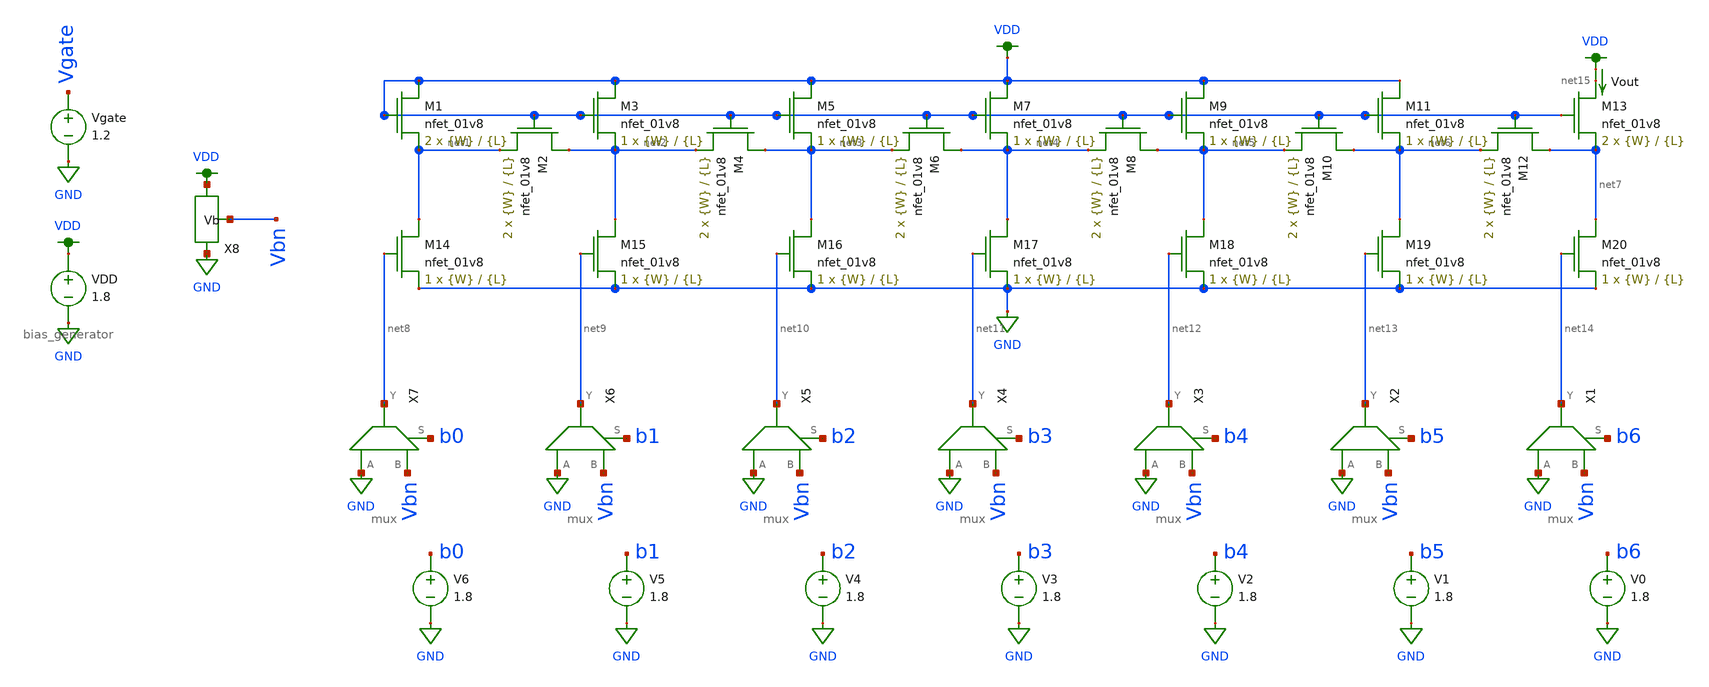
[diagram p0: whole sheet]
** sch_path: dac/schematics/misc/dac_dnl_inl.sch
**.subckt dac_dnl_inl
XM1 VDD VDD net1 GND sky130_fd_pr__nfet_01v8 L={L} W={W} nf=1 ad='int((nf+1)/2) * W/nf * 0.29' as='int((nf+2)/2) * W/nf * 0.29'
+ pd='2*int((nf+1)/2) * (W/nf + 0.29)' ps='2*int((nf+2)/2) * (W/nf + 0.29)' nrd='0.29 / W' nrs='0.29 / W'
+ sa=0 sb=0 sd=0 mult=2 m=2
XM2 net2 VDD net1 GND sky130_fd_pr__nfet_01v8 L={L} W={W} nf=1 ad='int((nf+1)/2) * W/nf * 0.29' as='int((nf+2)/2) * W/nf * 0.29'
+ pd='2*int((nf+1)/2) * (W/nf + 0.29)' ps='2*int((nf+2)/2) * (W/nf + 0.29)' nrd='0.29 / W' nrs='0.29 / W'
+ sa=0 sb=0 sd=0 mult=2 m=2
XM3 VDD VDD net2 GND sky130_fd_pr__nfet_01v8 L={L} W={W} nf=1 ad='int((nf+1)/2) * W/nf * 0.29' as='int((nf+2)/2) * W/nf * 0.29'
+ pd='2*int((nf+1)/2) * (W/nf + 0.29)' ps='2*int((nf+2)/2) * (W/nf + 0.29)' nrd='0.29 / W' nrs='0.29 / W'
+ sa=0 sb=0 sd=0 mult=1 m=1
XM4 net3 VDD net2 GND sky130_fd_pr__nfet_01v8 L={L} W={W} nf=1 ad='int((nf+1)/2) * W/nf * 0.29' as='int((nf+2)/2) * W/nf * 0.29'
+ pd='2*int((nf+1)/2) * (W/nf + 0.29)' ps='2*int((nf+2)/2) * (W/nf + 0.29)' nrd='0.29 / W' nrs='0.29 / W'
+ sa=0 sb=0 sd=0 mult=2 m=2
XM5 VDD VDD net3 GND sky130_fd_pr__nfet_01v8 L={L} W={W} nf=1 ad='int((nf+1)/2) * W/nf * 0.29' as='int((nf+2)/2) * W/nf * 0.29'
+ pd='2*int((nf+1)/2) * (W/nf + 0.29)' ps='2*int((nf+2)/2) * (W/nf + 0.29)' nrd='0.29 / W' nrs='0.29 / W'
+ sa=0 sb=0 sd=0 mult=1 m=1
XM6 net4 VDD net3 GND sky130_fd_pr__nfet_01v8 L={L} W={W} nf=1 ad='int((nf+1)/2) * W/nf * 0.29' as='int((nf+2)/2) * W/nf * 0.29'
+ pd='2*int((nf+1)/2) * (W/nf + 0.29)' ps='2*int((nf+2)/2) * (W/nf + 0.29)' nrd='0.29 / W' nrs='0.29 / W'
+ sa=0 sb=0 sd=0 mult=2 m=2
XM7 VDD VDD net4 GND sky130_fd_pr__nfet_01v8 L={L} W={W} nf=1 ad='int((nf+1)/2) * W/nf * 0.29' as='int((nf+2)/2) * W/nf * 0.29'
+ pd='2*int((nf+1)/2) * (W/nf + 0.29)' ps='2*int((nf+2)/2) * (W/nf + 0.29)' nrd='0.29 / W' nrs='0.29 / W'
+ sa=0 sb=0 sd=0 mult=1 m=1
XM8 net5 VDD net4 GND sky130_fd_pr__nfet_01v8 L={L} W={W} nf=1 ad='int((nf+1)/2) * W/nf * 0.29' as='int((nf+2)/2) * W/nf * 0.29'
+ pd='2*int((nf+1)/2) * (W/nf + 0.29)' ps='2*int((nf+2)/2) * (W/nf + 0.29)' nrd='0.29 / W' nrs='0.29 / W'
+ sa=0 sb=0 sd=0 mult=2 m=2
XM9 VDD VDD net5 GND sky130_fd_pr__nfet_01v8 L={L} W={W} nf=1 ad='int((nf+1)/2) * W/nf * 0.29' as='int((nf+2)/2) * W/nf * 0.29'
+ pd='2*int((nf+1)/2) * (W/nf + 0.29)' ps='2*int((nf+2)/2) * (W/nf + 0.29)' nrd='0.29 / W' nrs='0.29 / W'
+ sa=0 sb=0 sd=0 mult=1 m=1
XM10 net6 VDD net5 GND sky130_fd_pr__nfet_01v8 L={L} W={W} nf=1 ad='int((nf+1)/2) * W/nf * 0.29' as='int((nf+2)/2) * W/nf * 0.29'
+ pd='2*int((nf+1)/2) * (W/nf + 0.29)' ps='2*int((nf+2)/2) * (W/nf + 0.29)' nrd='0.29 / W' nrs='0.29 / W'
+ sa=0 sb=0 sd=0 mult=2 m=2
XM11 VDD VDD net6 GND sky130_fd_pr__nfet_01v8 L={L} W={W} nf=1 ad='int((nf+1)/2) * W/nf * 0.29' as='int((nf+2)/2) * W/nf * 0.29'
+ pd='2*int((nf+1)/2) * (W/nf + 0.29)' ps='2*int((nf+2)/2) * (W/nf + 0.29)' nrd='0.29 / W' nrs='0.29 / W'
+ sa=0 sb=0 sd=0 mult=1 m=1
XM12 net7 VDD net6 GND sky130_fd_pr__nfet_01v8 L={L} W={W} nf=1 ad='int((nf+1)/2) * W/nf * 0.29' as='int((nf+2)/2) * W/nf * 0.29'
+ pd='2*int((nf+1)/2) * (W/nf + 0.29)' ps='2*int((nf+2)/2) * (W/nf + 0.29)' nrd='0.29 / W' nrs='0.29 / W'
+ sa=0 sb=0 sd=0 mult=2 m=2
XM13 net15 VDD net7 GND sky130_fd_pr__nfet_01v8 L={L} W={W} nf=1 ad='int((nf+1)/2) * W/nf * 0.29' as='int((nf+2)/2) * W/nf * 0.29'
+ pd='2*int((nf+1)/2) * (W/nf + 0.29)' ps='2*int((nf+2)/2) * (W/nf + 0.29)' nrd='0.29 / W' nrs='0.29 / W'
+ sa=0 sb=0 sd=0 mult=2 m=2
XM14 net1 net8 GND GND sky130_fd_pr__nfet_01v8 L={L} W={W} nf=1 ad='int((nf+1)/2) * W/nf * 0.29' as='int((nf+2)/2) * W/nf * 0.29'
+ pd='2*int((nf+1)/2) * (W/nf + 0.29)' ps='2*int((nf+2)/2) * (W/nf + 0.29)' nrd='0.29 / W' nrs='0.29 / W'
+ sa=0 sb=0 sd=0 mult=1 m=1
XM15 net2 net9 GND GND sky130_fd_pr__nfet_01v8 L={L} W={W} nf=1 ad='int((nf+1)/2) * W/nf * 0.29' as='int((nf+2)/2) * W/nf * 0.29'
+ pd='2*int((nf+1)/2) * (W/nf + 0.29)' ps='2*int((nf+2)/2) * (W/nf + 0.29)' nrd='0.29 / W' nrs='0.29 / W'
+ sa=0 sb=0 sd=0 mult=1 m=1
XM16 net3 net10 GND GND sky130_fd_pr__nfet_01v8 L={L} W={W} nf=1 ad='int((nf+1)/2) * W/nf * 0.29' as='int((nf+2)/2) * W/nf * 0.29'
+ pd='2*int((nf+1)/2) * (W/nf + 0.29)' ps='2*int((nf+2)/2) * (W/nf + 0.29)' nrd='0.29 / W' nrs='0.29 / W'
+ sa=0 sb=0 sd=0 mult=1 m=1
XM17 net4 net11 GND GND sky130_fd_pr__nfet_01v8 L={L} W={W} nf=1 ad='int((nf+1)/2) * W/nf * 0.29' as='int((nf+2)/2) * W/nf * 0.29'
+ pd='2*int((nf+1)/2) * (W/nf + 0.29)' ps='2*int((nf+2)/2) * (W/nf + 0.29)' nrd='0.29 / W' nrs='0.29 / W'
+ sa=0 sb=0 sd=0 mult=1 m=1
XM18 net5 net12 GND GND sky130_fd_pr__nfet_01v8 L={L} W={W} nf=1 ad='int((nf+1)/2) * W/nf * 0.29' as='int((nf+2)/2) * W/nf * 0.29'
+ pd='2*int((nf+1)/2) * (W/nf + 0.29)' ps='2*int((nf+2)/2) * (W/nf + 0.29)' nrd='0.29 / W' nrs='0.29 / W'
+ sa=0 sb=0 sd=0 mult=1 m=1
XM19 net6 net13 GND GND sky130_fd_pr__nfet_01v8 L={L} W={W} nf=1 ad='int((nf+1)/2) * W/nf * 0.29' as='int((nf+2)/2) * W/nf * 0.29'
+ pd='2*int((nf+1)/2) * (W/nf + 0.29)' ps='2*int((nf+2)/2) * (W/nf + 0.29)' nrd='0.29 / W' nrs='0.29 / W'
+ sa=0 sb=0 sd=0 mult=1 m=1
XM20 net7 net14 GND GND sky130_fd_pr__nfet_01v8 L={L} W={W} nf=1 ad='int((nf+1)/2) * W/nf * 0.29' as='int((nf+2)/2) * W/nf * 0.29'
+ pd='2*int((nf+1)/2) * (W/nf + 0.29)' ps='2*int((nf+2)/2) * (W/nf + 0.29)' nrd='0.29 / W' nrs='0.29 / W'
+ sa=0 sb=0 sd=0 mult=1 m=1
Vgate Vgate GND 1.2
X1 GND Vbn net14 b6 mux
X2 GND Vbn net13 b5 mux
X3 GND Vbn net12 b4 mux
X4 GND Vbn net11 b3 mux
X5 GND Vbn net10 b2 mux
X6 GND Vbn net9 b1 mux
X7 GND Vbn net8 b0 mux
V0 b6 GND 1.8
V1 b5 GND 1.8
V2 b4 GND 1.8
V3 b3 GND 1.8
V4 b2 GND 1.8
V5 b1 GND 1.8
V6 b0 GND 1.8
Vout VDD net15 0
.save i(vout)
VDD VDD GND 1.8
X8 VDD GND Vbn bias_generator
**** begin user architecture code

.param W=1
.param L=0.5
.control
set wr_vecnames
set wr_singlescale
let code = 0
  while code < 128
    if code eq 0
      let b0 = 0
    else
      let b0 = code % 2
    end
    if floor(code / 2) eq 0
      let b1 = 0
    else
      let b1 = floor(code / 2) % 2
    end
    if floor(code / 4) eq 0
      let b2 = 0
    else
      let b2 = floor(code / 4) % 2
    end
    if floor(code / 8) eq 0
      let b3 = 0
    else
      let b3 = floor(code / 8) % 2
    end
    if floor(code / 16) eq 0
      let b4 = 0
    else
      let b4 = floor(code / 16) % 2
    end
    if floor(code / 32) eq 0
      let b5 = 0
    else
      let b5 = floor(code / 32) % 2
    end
    if floor(code / 64) eq 0
      let b6 = 0
    else
      let b6 = floor(code / 64) % 2
    end
    alter v0 $&b0
    alter v1 $&b1
    alter v2 $&b2
    alter v3 $&b3
    alter v4 $&b4
    alter v5 $&b5
    alter v6 $&b6
    save all
    op
    wrdata ~/Documents/current-output-dac-vlsi/simulations/dac_inf_sim.txt i(Vout) v(b5) v(b6)
    if code eq 0
      set appendwrite
      set wr_vecnames = FALSE
    end
    let code = code + 1
  end
  quit
.endc


.option wnflag=1
.param MC_SWITCH=0.0
.lib ~/skywater/skywater-pdk/libraries/sky130_fd_pr_ngspice/latest/models/sky130.lib.spice tt

**** end user architecture code
**.ends

* expanding   symbol:  /home/madvlsi/Documents/current-output-dac-vlsi/schematics/mux.sym # of
*+ pins=4
** sym_path: dac/schematics/mux.sym
** sch_path: dac/schematics/mux.sch
.subckt mux A B Y S
*.ipin A
*.ipin B
*.ipin S
*.opin Y
XM1 A S Y VDD sky130_fd_pr__pfet_01v8 L=0.15 W=1 nf=1 ad='int((nf+1)/2) * W/nf * 0.29' as='int((nf+2)/2) * W/nf * 0.29'
+ pd='2*int((nf+1)/2) * (W/nf + 0.29)' ps='2*int((nf+2)/2) * (W/nf + 0.29)' nrd='0.29 / W' nrs='0.29 / W'
+ sa=0 sb=0 sd=0 mult=1 m=1
XM3 net1 S VDD VDD sky130_fd_pr__pfet_01v8 L=0.15 W=1 nf=1 ad='int((nf+1)/2) * W/nf * 0.29' as='int((nf+2)/2) * W/nf * 0.29'
+ pd='2*int((nf+1)/2) * (W/nf + 0.29)' ps='2*int((nf+2)/2) * (W/nf + 0.29)' nrd='0.29 / W' nrs='0.29 / W'
+ sa=0 sb=0 sd=0 mult=1 m=1
XM4 net1 S GND GND sky130_fd_pr__nfet_01v8 L=0.15 W=1 nf=1 ad='int((nf+1)/2) * W/nf * 0.29' as='int((nf+2)/2) * W/nf * 0.29'
+ pd='2*int((nf+1)/2) * (W/nf + 0.29)' ps='2*int((nf+2)/2) * (W/nf + 0.29)' nrd='0.29 / W' nrs='0.29 / W'
+ sa=0 sb=0 sd=0 mult=1 m=1
XM5 A net1 Y GND sky130_fd_pr__nfet_01v8 L=0.15 W=1 nf=1 ad='int((nf+1)/2) * W/nf * 0.29' as='int((nf+2)/2) * W/nf * 0.29'
+ pd='2*int((nf+1)/2) * (W/nf + 0.29)' ps='2*int((nf+2)/2) * (W/nf + 0.29)' nrd='0.29 / W' nrs='0.29 / W'
+ sa=0 sb=0 sd=0 mult=1 m=1
XM2 B net1 Y VDD sky130_fd_pr__pfet_01v8 L=0.15 W=1 nf=1 ad='int((nf+1)/2) * W/nf * 0.29' as='int((nf+2)/2) * W/nf * 0.29'
+ pd='2*int((nf+1)/2) * (W/nf + 0.29)' ps='2*int((nf+2)/2) * (W/nf + 0.29)' nrd='0.29 / W' nrs='0.29 / W'
+ sa=0 sb=0 sd=0 mult=1 m=1
XM6 B S Y GND sky130_fd_pr__nfet_01v8 L=0.15 W=1 nf=1 ad='int((nf+1)/2) * W/nf * 0.29' as='int((nf+2)/2) * W/nf * 0.29'
+ pd='2*int((nf+1)/2) * (W/nf + 0.29)' ps='2*int((nf+2)/2) * (W/nf + 0.29)' nrd='0.29 / W' nrs='0.29 / W'
+ sa=0 sb=0 sd=0 mult=1 m=1
.ends


* expanding   symbol:  /home/madvlsi/Documents/current-output-dac-vlsi/schematics/bias_generator.sym
*+ # of pins=3
** sym_path: dac/schematics/bias_generator.sym
** sch_path: dac/schematics/bias_generator.sch
.subckt bias_generator VP VN Vb
*.iopin VP
*.iopin VN
*.opin Vb
XM20 VP net2 net3 VDD sky130_fd_pr__pfet_01v8 L=0.5 W=1 nf=1 ad='int((nf+1)/2) * W/nf * 0.29' as='int((nf+2)/2) * W/nf * 0.29'
+ pd='2*int((nf+1)/2) * (W/nf + 0.29)' ps='2*int((nf+2)/2) * (W/nf + 0.29)' nrd='0.29 / W' nrs='0.29 / W'
+ sa=0 sb=0 sd=0 mult=1 m=1
XM21 net4 net3 net3 GND sky130_fd_pr__nfet_01v8 L=0.5 W=1 nf=1 ad='int((nf+1)/2) * W/nf * 0.29' as='int((nf+2)/2) * W/nf * 0.29'
+ pd='2*int((nf+1)/2) * (W/nf + 0.29)' ps='2*int((nf+2)/2) * (W/nf + 0.29)' nrd='0.29 / W' nrs='0.29 / W'
+ sa=0 sb=0 sd=0 mult=8 m=8
R3 net4 VN 400k m=1
XM22 net1 net3 VN GND sky130_fd_pr__nfet_01v8 L=0.5 W=1 nf=1 ad='int((nf+1)/2) * W/nf * 0.29' as='int((nf+2)/2) * W/nf * 0.29'
+ pd='2*int((nf+1)/2) * (W/nf + 0.29)' ps='2*int((nf+2)/2) * (W/nf + 0.29)' nrd='0.29 / W' nrs='0.29 / W'
+ sa=0 sb=0 sd=0 mult=1 m=1
XM23 VN Vb net2 GND sky130_fd_pr__nfet_01v8 L=0.5 W=1 nf=1 ad='int((nf+1)/2) * W/nf * 0.29' as='int((nf+2)/2) * W/nf * 0.29'
+ pd='2*int((nf+1)/2) * (W/nf + 0.29)' ps='2*int((nf+2)/2) * (W/nf + 0.29)' nrd='0.29 / W' nrs='0.29 / W'
+ sa=0 sb=0 sd=0 mult=1 m=1
XM24 Vb Vb VN GND sky130_fd_pr__nfet_01v8 L=0.5 W=1 nf=1 ad='int((nf+1)/2) * W/nf * 0.29' as='int((nf+2)/2) * W/nf * 0.29'
+ pd='2*int((nf+1)/2) * (W/nf + 0.29)' ps='2*int((nf+2)/2) * (W/nf + 0.29)' nrd='0.29 / W' nrs='0.29 / W'
+ sa=0 sb=0 sd=0 mult=1 m=1
XM25 VP net1 net1 VDD sky130_fd_pr__pfet_01v8 L=0.5 W=1 nf=1 ad='int((nf+1)/2) * W/nf * 0.29' as='int((nf+2)/2) * W/nf * 0.29'
+ pd='2*int((nf+1)/2) * (W/nf + 0.29)' ps='2*int((nf+2)/2) * (W/nf + 0.29)' nrd='0.29 / W' nrs='0.29 / W'
+ sa=0 sb=0 sd=0 mult=1 m=1
XM26 net2 net1 VP VDD sky130_fd_pr__pfet_01v8 L=0.5 W=1 nf=1 ad='int((nf+1)/2) * W/nf * 0.29' as='int((nf+2)/2) * W/nf * 0.29'
+ pd='2*int((nf+1)/2) * (W/nf + 0.29)' ps='2*int((nf+2)/2) * (W/nf + 0.29)' nrd='0.29 / W' nrs='0.29 / W'
+ sa=0 sb=0 sd=0 mult=1 m=1
XM27 Vb net2 VP VDD sky130_fd_pr__pfet_01v8 L=0.5 W=1 nf=1 ad='int((nf+1)/2) * W/nf * 0.29' as='int((nf+2)/2) * W/nf * 0.29'
+ pd='2*int((nf+1)/2) * (W/nf + 0.29)' ps='2*int((nf+2)/2) * (W/nf + 0.29)' nrd='0.29 / W' nrs='0.29 / W'
+ sa=0 sb=0 sd=0 mult=1 m=1
.ends

.GLOBAL GND
.GLOBAL VDD
.end
